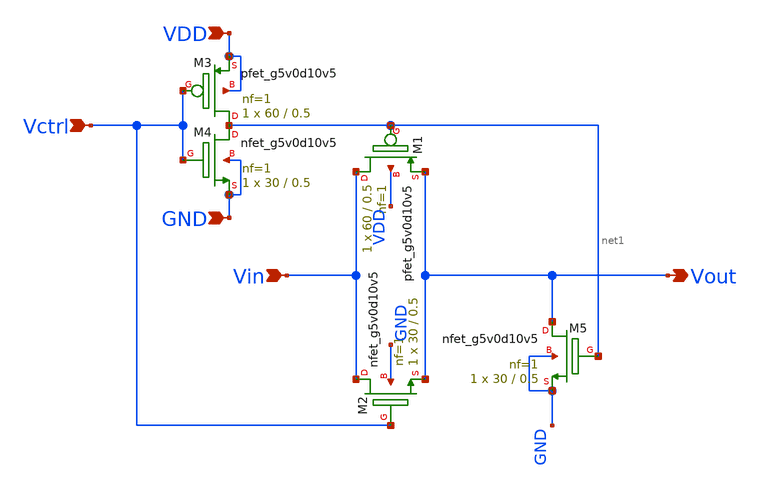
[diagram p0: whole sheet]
** sch_path: xschem/SW_CDAC.sch
**.subckt SW_CDAC Vctrl Vin Vout VDD GND
*.ipin Vctrl
*.ipin Vin
*.opin Vout
*.ipin VDD
*.ipin GND
XM1 Vin net1 Vout VDD sky130_fd_pr__pfet_g5v0d10v5 L=0.5 W=60 nf=1 ad='int((1 + 1)/2) * 60 / 1 * 0.29'
+ as='int((1 + 2)/2) * 60 / 1 * 0.29' pd='2*int((1 + 1)/2) * (60 / 1 + 0.29)' ps='2*int((1 + 2)/2) * (60 / 1 + 0.29)'
+ nrd='0.29 / 60 ' nrs='0.29 / 60 ' sa=0 sb=0 sd=0 mult=1 m=1
XM2 Vin Vctrl Vout GND sky130_fd_pr__nfet_g5v0d10v5 L=0.5 W=30 nf=1 ad='int((1 + 1)/2) * 30 / 1 * 0.29'
+ as='int((1 + 2)/2) * 30 / 1 * 0.29' pd='2*int((1 + 1)/2) * (30 / 1 + 0.29)' ps='2*int((1 + 2)/2) * (30 / 1 + 0.29)'
+ nrd='0.29 / 30 ' nrs='0.29 / 30 ' sa=0 sb=0 sd=0 mult=1 m=1
XM3 net1 Vctrl VDD VDD sky130_fd_pr__pfet_g5v0d10v5 L=0.5 W=60 nf=1 ad='int((1 + 1)/2) * 60 / 1 * 0.29'
+ as='int((1 + 2)/2) * 60 / 1 * 0.29' pd='2*int((1 + 1)/2) * (60 / 1 + 0.29)' ps='2*int((1 + 2)/2) * (60 / 1 + 0.29)'
+ nrd='0.29 / 60 ' nrs='0.29 / 60 ' sa=0 sb=0 sd=0 mult=1 m=1
XM4 net1 Vctrl GND GND sky130_fd_pr__nfet_g5v0d10v5 L=0.5 W=30 nf=1 ad='int((1 + 1)/2) * 30 / 1 * 0.29'
+ as='int((1 + 2)/2) * 30 / 1 * 0.29' pd='2*int((1 + 1)/2) * (30 / 1 + 0.29)' ps='2*int((1 + 2)/2) * (30 / 1 + 0.29)'
+ nrd='0.29 / 30 ' nrs='0.29 / 30 ' sa=0 sb=0 sd=0 mult=1 m=1
XM5 Vout net1 GND GND sky130_fd_pr__nfet_g5v0d10v5 L=0.5 W=30 nf=1 ad='int((1 + 1)/2) * 30 / 1 * 0.29'
+ as='int((1 + 2)/2) * 30 / 1 * 0.29' pd='2*int((1 + 1)/2) * (30 / 1 + 0.29)' ps='2*int((1 + 2)/2) * (30 / 1 + 0.29)'
+ nrd='0.29 / 30 ' nrs='0.29 / 30 ' sa=0 sb=0 sd=0 mult=1 m=1
**.ends
.end
